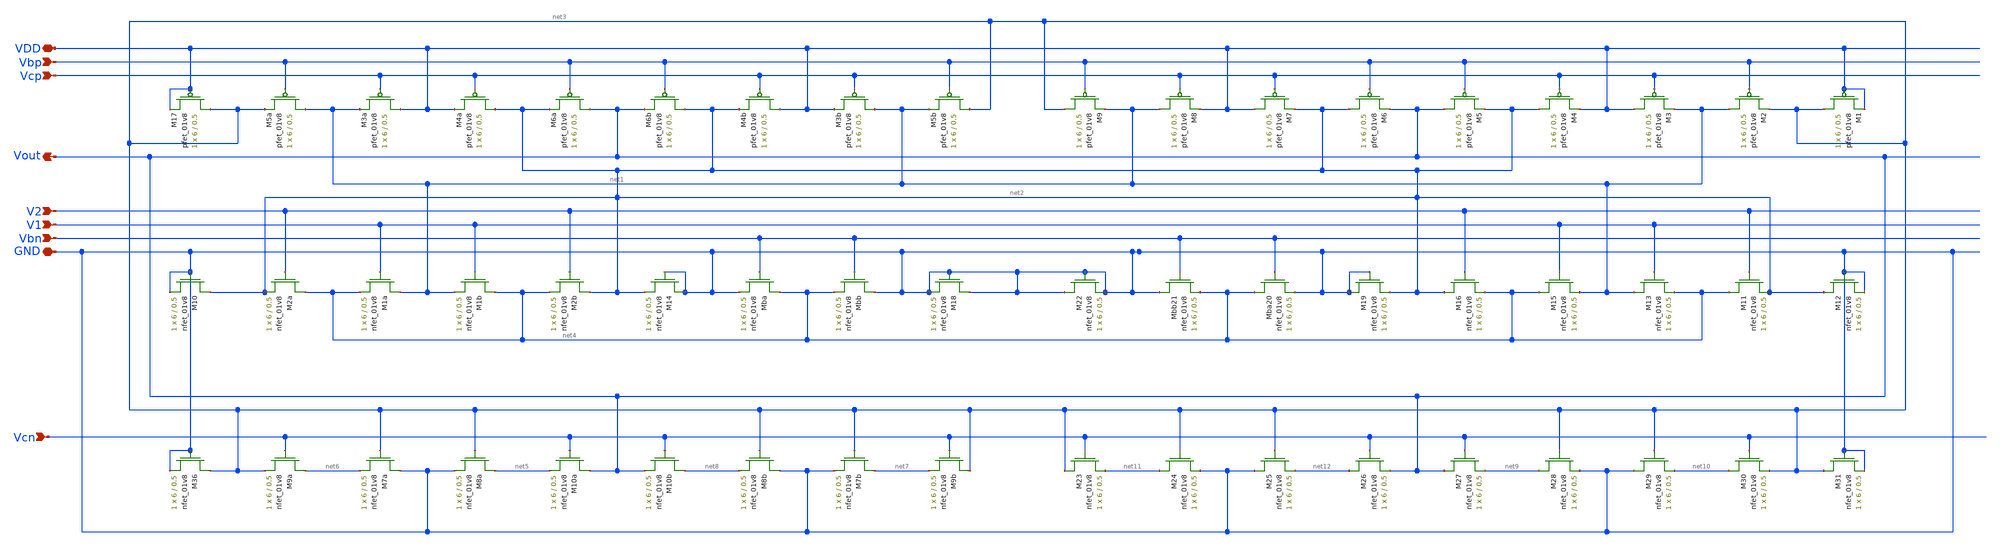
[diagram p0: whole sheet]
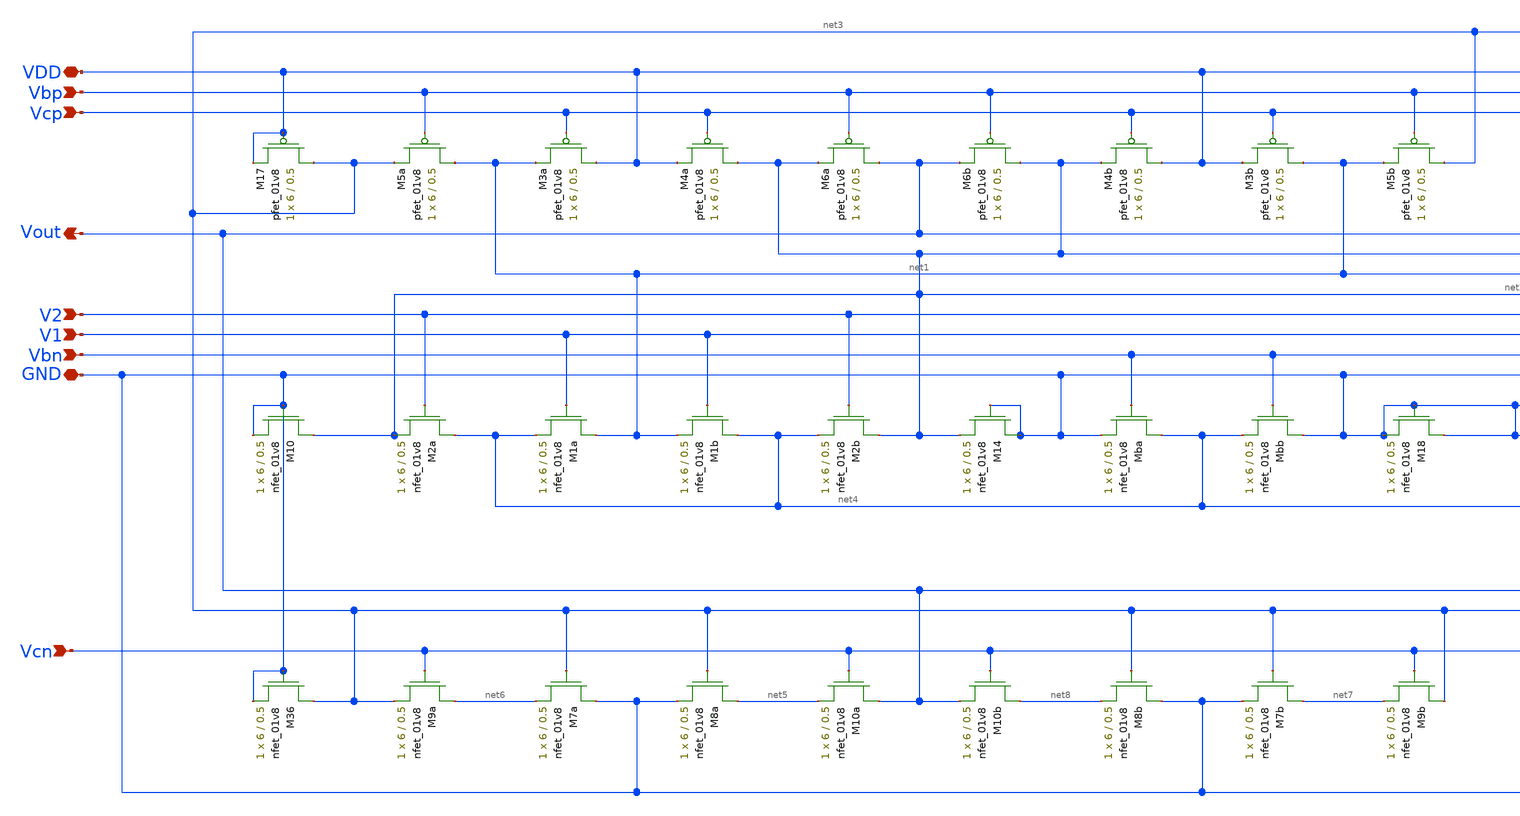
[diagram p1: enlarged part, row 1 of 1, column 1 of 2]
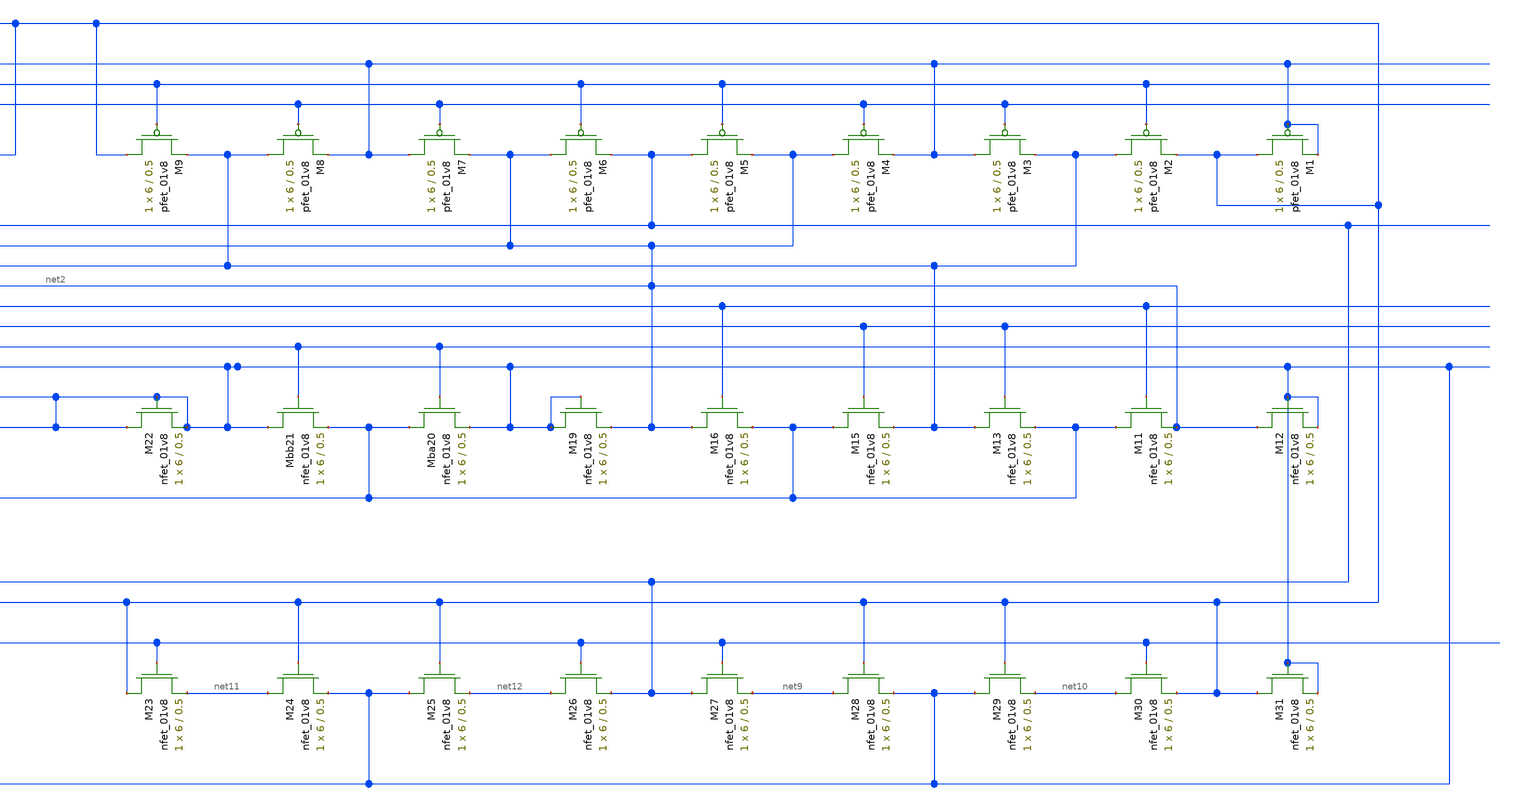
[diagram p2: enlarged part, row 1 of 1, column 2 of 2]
** sch_path: Miniproject3/layout&schematics/LDS_simple.sch
**.subckt LDS_simple Vbp Vout V2 Vbn VDD GND Vcn Vcp V1
*.ipin Vbp
*.opin Vout
*.ipin V2
*.ipin Vbn
*.iopin VDD
*.iopin GND
*.ipin Vcn
*.ipin Vcp
*.ipin V1
XM17 net3 VDD VDD VDD sky130_fd_pr__pfet_01v8 L=0.5 W=6 nf=1 ad='int((nf+1)/2) * W/nf * 0.29' as='int((nf+2)/2) * W/nf * 0.29'
+ pd='2*int((nf+1)/2) * (W/nf + 0.29)' ps='2*int((nf+2)/2) * (W/nf + 0.29)' nrd='0.29 / W' nrs='0.29 / W'
+ sa=0 sb=0 sd=0 mult=1 m=1
XM5a net1 Vbp net3 VDD sky130_fd_pr__pfet_01v8 L=0.5 W=6 nf=1 ad='int((nf+1)/2) * W/nf * 0.29' as='int((nf+2)/2) * W/nf * 0.29'
+ pd='2*int((nf+1)/2) * (W/nf + 0.29)' ps='2*int((nf+2)/2) * (W/nf + 0.29)' nrd='0.29 / W' nrs='0.29 / W'
+ sa=0 sb=0 sd=0 mult=1 m=1
XM3a VDD Vcp net1 VDD sky130_fd_pr__pfet_01v8 L=0.5 W=6 nf=1 ad='int((nf+1)/2) * W/nf * 0.29' as='int((nf+2)/2) * W/nf * 0.29'
+ pd='2*int((nf+1)/2) * (W/nf + 0.29)' ps='2*int((nf+2)/2) * (W/nf + 0.29)' nrd='0.29 / W' nrs='0.29 / W'
+ sa=0 sb=0 sd=0 mult=1 m=1
XM4a net2 Vcp VDD VDD sky130_fd_pr__pfet_01v8 L=0.5 W=6 nf=1 ad='int((nf+1)/2) * W/nf * 0.29' as='int((nf+2)/2) * W/nf * 0.29'
+ pd='2*int((nf+1)/2) * (W/nf + 0.29)' ps='2*int((nf+2)/2) * (W/nf + 0.29)' nrd='0.29 / W' nrs='0.29 / W'
+ sa=0 sb=0 sd=0 mult=1 m=1
XM6a Vout Vbp net2 VDD sky130_fd_pr__pfet_01v8 L=0.5 W=6 nf=1 ad='int((nf+1)/2) * W/nf * 0.29' as='int((nf+2)/2) * W/nf * 0.29'
+ pd='2*int((nf+1)/2) * (W/nf + 0.29)' ps='2*int((nf+2)/2) * (W/nf + 0.29)' nrd='0.29 / W' nrs='0.29 / W'
+ sa=0 sb=0 sd=0 mult=1 m=1
XM6b net2 Vbp Vout VDD sky130_fd_pr__pfet_01v8 L=0.5 W=6 nf=1 ad='int((nf+1)/2) * W/nf * 0.29' as='int((nf+2)/2) * W/nf * 0.29'
+ pd='2*int((nf+1)/2) * (W/nf + 0.29)' ps='2*int((nf+2)/2) * (W/nf + 0.29)' nrd='0.29 / W' nrs='0.29 / W'
+ sa=0 sb=0 sd=0 mult=1 m=1
XM4b VDD Vcp net2 VDD sky130_fd_pr__pfet_01v8 L=0.5 W=6 nf=1 ad='int((nf+1)/2) * W/nf * 0.29' as='int((nf+2)/2) * W/nf * 0.29'
+ pd='2*int((nf+1)/2) * (W/nf + 0.29)' ps='2*int((nf+2)/2) * (W/nf + 0.29)' nrd='0.29 / W' nrs='0.29 / W'
+ sa=0 sb=0 sd=0 mult=1 m=1
XM3b net1 Vcp VDD VDD sky130_fd_pr__pfet_01v8 L=0.5 W=6 nf=1 ad='int((nf+1)/2) * W/nf * 0.29' as='int((nf+2)/2) * W/nf * 0.29'
+ pd='2*int((nf+1)/2) * (W/nf + 0.29)' ps='2*int((nf+2)/2) * (W/nf + 0.29)' nrd='0.29 / W' nrs='0.29 / W'
+ sa=0 sb=0 sd=0 mult=1 m=1
XM5b net3 Vbp net1 VDD sky130_fd_pr__pfet_01v8 L=0.5 W=6 nf=1 ad='int((nf+1)/2) * W/nf * 0.29' as='int((nf+2)/2) * W/nf * 0.29'
+ pd='2*int((nf+1)/2) * (W/nf + 0.29)' ps='2*int((nf+2)/2) * (W/nf + 0.29)' nrd='0.29 / W' nrs='0.29 / W'
+ sa=0 sb=0 sd=0 mult=1 m=1
XM2a net4 V2 net2 GND sky130_fd_pr__nfet_01v8 L=0.5 W=6 nf=1 ad='int((nf+1)/2) * W/nf * 0.29' as='int((nf+2)/2) * W/nf * 0.29'
+ pd='2*int((nf+1)/2) * (W/nf + 0.29)' ps='2*int((nf+2)/2) * (W/nf + 0.29)' nrd='0.29 / W' nrs='0.29 / W'
+ sa=0 sb=0 sd=0 mult=1 m=1
XM10 net2 GND GND GND sky130_fd_pr__nfet_01v8 L=0.5 W=6 nf=1 ad='int((nf+1)/2) * W/nf * 0.29' as='int((nf+2)/2) * W/nf * 0.29'
+ pd='2*int((nf+1)/2) * (W/nf + 0.29)' ps='2*int((nf+2)/2) * (W/nf + 0.29)' nrd='0.29 / W' nrs='0.29 / W'
+ sa=0 sb=0 sd=0 mult=1 m=1
XM1a net1 V1 net4 GND sky130_fd_pr__nfet_01v8 L=0.5 W=6 nf=1 ad='int((nf+1)/2) * W/nf * 0.29' as='int((nf+2)/2) * W/nf * 0.29'
+ pd='2*int((nf+1)/2) * (W/nf + 0.29)' ps='2*int((nf+2)/2) * (W/nf + 0.29)' nrd='0.29 / W' nrs='0.29 / W'
+ sa=0 sb=0 sd=0 mult=1 m=1
XM1b net4 V1 net1 GND sky130_fd_pr__nfet_01v8 L=0.5 W=6 nf=1 ad='int((nf+1)/2) * W/nf * 0.29' as='int((nf+2)/2) * W/nf * 0.29'
+ pd='2*int((nf+1)/2) * (W/nf + 0.29)' ps='2*int((nf+2)/2) * (W/nf + 0.29)' nrd='0.29 / W' nrs='0.29 / W'
+ sa=0 sb=0 sd=0 mult=1 m=1
XM2b net2 V2 net4 GND sky130_fd_pr__nfet_01v8 L=0.5 W=6 nf=1 ad='int((nf+1)/2) * W/nf * 0.29' as='int((nf+2)/2) * W/nf * 0.29'
+ pd='2*int((nf+1)/2) * (W/nf + 0.29)' ps='2*int((nf+2)/2) * (W/nf + 0.29)' nrd='0.29 / W' nrs='0.29 / W'
+ sa=0 sb=0 sd=0 mult=1 m=1
XM14 GND GND net2 GND sky130_fd_pr__nfet_01v8 L=0.5 W=6 nf=1 ad='int((nf+1)/2) * W/nf * 0.29' as='int((nf+2)/2) * W/nf * 0.29'
+ pd='2*int((nf+1)/2) * (W/nf + 0.29)' ps='2*int((nf+2)/2) * (W/nf + 0.29)' nrd='0.29 / W' nrs='0.29 / W'
+ sa=0 sb=0 sd=0 mult=1 m=1
XMba net4 Vbn GND GND sky130_fd_pr__nfet_01v8 L=0.5 W=6 nf=1 ad='int((nf+1)/2) * W/nf * 0.29' as='int((nf+2)/2) * W/nf * 0.29'
+ pd='2*int((nf+1)/2) * (W/nf + 0.29)' ps='2*int((nf+2)/2) * (W/nf + 0.29)' nrd='0.29 / W' nrs='0.29 / W'
+ sa=0 sb=0 sd=0 mult=1 m=1
XMbb GND Vbn net4 GND sky130_fd_pr__nfet_01v8 L=0.5 W=6 nf=1 ad='int((nf+1)/2) * W/nf * 0.29' as='int((nf+2)/2) * W/nf * 0.29'
+ pd='2*int((nf+1)/2) * (W/nf + 0.29)' ps='2*int((nf+2)/2) * (W/nf + 0.29)' nrd='0.29 / W' nrs='0.29 / W'
+ sa=0 sb=0 sd=0 mult=1 m=1
XM18 GND GND GND GND sky130_fd_pr__nfet_01v8 L=0.5 W=6 nf=1 ad='int((nf+1)/2) * W/nf * 0.29' as='int((nf+2)/2) * W/nf * 0.29'
+ pd='2*int((nf+1)/2) * (W/nf + 0.29)' ps='2*int((nf+2)/2) * (W/nf + 0.29)' nrd='0.29 / W' nrs='0.29 / W'
+ sa=0 sb=0 sd=0 mult=1 m=1
XM9b net3 Vcn net7 GND sky130_fd_pr__nfet_01v8 L=0.5 W=6 nf=1 ad='int((nf+1)/2) * W/nf * 0.29' as='int((nf+2)/2) * W/nf * 0.29'
+ pd='2*int((nf+1)/2) * (W/nf + 0.29)' ps='2*int((nf+2)/2) * (W/nf + 0.29)' nrd='0.29 / W' nrs='0.29 / W'
+ sa=0 sb=0 sd=0 mult=1 m=1
XM7b net7 net3 GND GND sky130_fd_pr__nfet_01v8 L=0.5 W=6 nf=1 ad='int((nf+1)/2) * W/nf * 0.29' as='int((nf+2)/2) * W/nf * 0.29'
+ pd='2*int((nf+1)/2) * (W/nf + 0.29)' ps='2*int((nf+2)/2) * (W/nf + 0.29)' nrd='0.29 / W' nrs='0.29 / W'
+ sa=0 sb=0 sd=0 mult=1 m=1
XM8b GND net3 net8 GND sky130_fd_pr__nfet_01v8 L=0.5 W=6 nf=1 ad='int((nf+1)/2) * W/nf * 0.29' as='int((nf+2)/2) * W/nf * 0.29'
+ pd='2*int((nf+1)/2) * (W/nf + 0.29)' ps='2*int((nf+2)/2) * (W/nf + 0.29)' nrd='0.29 / W' nrs='0.29 / W'
+ sa=0 sb=0 sd=0 mult=1 m=1
XM10b net8 Vcn Vout GND sky130_fd_pr__nfet_01v8 L=0.5 W=6 nf=1 ad='int((nf+1)/2) * W/nf * 0.29' as='int((nf+2)/2) * W/nf * 0.29'
+ pd='2*int((nf+1)/2) * (W/nf + 0.29)' ps='2*int((nf+2)/2) * (W/nf + 0.29)' nrd='0.29 / W' nrs='0.29 / W'
+ sa=0 sb=0 sd=0 mult=1 m=1
XM10a Vout Vcn net5 GND sky130_fd_pr__nfet_01v8 L=0.5 W=6 nf=1 ad='int((nf+1)/2) * W/nf * 0.29' as='int((nf+2)/2) * W/nf * 0.29'
+ pd='2*int((nf+1)/2) * (W/nf + 0.29)' ps='2*int((nf+2)/2) * (W/nf + 0.29)' nrd='0.29 / W' nrs='0.29 / W'
+ sa=0 sb=0 sd=0 mult=1 m=1
XM8a net5 net3 GND GND sky130_fd_pr__nfet_01v8 L=0.5 W=6 nf=1 ad='int((nf+1)/2) * W/nf * 0.29' as='int((nf+2)/2) * W/nf * 0.29'
+ pd='2*int((nf+1)/2) * (W/nf + 0.29)' ps='2*int((nf+2)/2) * (W/nf + 0.29)' nrd='0.29 / W' nrs='0.29 / W'
+ sa=0 sb=0 sd=0 mult=1 m=1
XM7a GND net3 net6 GND sky130_fd_pr__nfet_01v8 L=0.5 W=6 nf=1 ad='int((nf+1)/2) * W/nf * 0.29' as='int((nf+2)/2) * W/nf * 0.29'
+ pd='2*int((nf+1)/2) * (W/nf + 0.29)' ps='2*int((nf+2)/2) * (W/nf + 0.29)' nrd='0.29 / W' nrs='0.29 / W'
+ sa=0 sb=0 sd=0 mult=1 m=1
XM9a net6 Vcn net3 GND sky130_fd_pr__nfet_01v8 L=0.5 W=6 nf=1 ad='int((nf+1)/2) * W/nf * 0.29' as='int((nf+2)/2) * W/nf * 0.29'
+ pd='2*int((nf+1)/2) * (W/nf + 0.29)' ps='2*int((nf+2)/2) * (W/nf + 0.29)' nrd='0.29 / W' nrs='0.29 / W'
+ sa=0 sb=0 sd=0 mult=1 m=1
XM36 net3 GND GND GND sky130_fd_pr__nfet_01v8 L=0.5 W=6 nf=1 ad='int((nf+1)/2) * W/nf * 0.29' as='int((nf+2)/2) * W/nf * 0.29'
+ pd='2*int((nf+1)/2) * (W/nf + 0.29)' ps='2*int((nf+2)/2) * (W/nf + 0.29)' nrd='0.29 / W' nrs='0.29 / W'
+ sa=0 sb=0 sd=0 mult=1 m=1
XM1 net3 VDD VDD VDD sky130_fd_pr__pfet_01v8 L=0.5 W=6 nf=1 ad='int((nf+1)/2) * W/nf * 0.29' as='int((nf+2)/2) * W/nf * 0.29'
+ pd='2*int((nf+1)/2) * (W/nf + 0.29)' ps='2*int((nf+2)/2) * (W/nf + 0.29)' nrd='0.29 / W' nrs='0.29 / W'
+ sa=0 sb=0 sd=0 mult=1 m=1
XM2 net1 Vbp net3 VDD sky130_fd_pr__pfet_01v8 L=0.5 W=6 nf=1 ad='int((nf+1)/2) * W/nf * 0.29' as='int((nf+2)/2) * W/nf * 0.29'
+ pd='2*int((nf+1)/2) * (W/nf + 0.29)' ps='2*int((nf+2)/2) * (W/nf + 0.29)' nrd='0.29 / W' nrs='0.29 / W'
+ sa=0 sb=0 sd=0 mult=1 m=1
XM3 VDD Vcp net1 VDD sky130_fd_pr__pfet_01v8 L=0.5 W=6 nf=1 ad='int((nf+1)/2) * W/nf * 0.29' as='int((nf+2)/2) * W/nf * 0.29'
+ pd='2*int((nf+1)/2) * (W/nf + 0.29)' ps='2*int((nf+2)/2) * (W/nf + 0.29)' nrd='0.29 / W' nrs='0.29 / W'
+ sa=0 sb=0 sd=0 mult=1 m=1
XM4 net2 Vcp VDD VDD sky130_fd_pr__pfet_01v8 L=0.5 W=6 nf=1 ad='int((nf+1)/2) * W/nf * 0.29' as='int((nf+2)/2) * W/nf * 0.29'
+ pd='2*int((nf+1)/2) * (W/nf + 0.29)' ps='2*int((nf+2)/2) * (W/nf + 0.29)' nrd='0.29 / W' nrs='0.29 / W'
+ sa=0 sb=0 sd=0 mult=1 m=1
XM5 Vout Vbp net2 VDD sky130_fd_pr__pfet_01v8 L=0.5 W=6 nf=1 ad='int((nf+1)/2) * W/nf * 0.29' as='int((nf+2)/2) * W/nf * 0.29'
+ pd='2*int((nf+1)/2) * (W/nf + 0.29)' ps='2*int((nf+2)/2) * (W/nf + 0.29)' nrd='0.29 / W' nrs='0.29 / W'
+ sa=0 sb=0 sd=0 mult=1 m=1
XM6 net2 Vbp Vout VDD sky130_fd_pr__pfet_01v8 L=0.5 W=6 nf=1 ad='int((nf+1)/2) * W/nf * 0.29' as='int((nf+2)/2) * W/nf * 0.29'
+ pd='2*int((nf+1)/2) * (W/nf + 0.29)' ps='2*int((nf+2)/2) * (W/nf + 0.29)' nrd='0.29 / W' nrs='0.29 / W'
+ sa=0 sb=0 sd=0 mult=1 m=1
XM7 VDD Vcp net2 VDD sky130_fd_pr__pfet_01v8 L=0.5 W=6 nf=1 ad='int((nf+1)/2) * W/nf * 0.29' as='int((nf+2)/2) * W/nf * 0.29'
+ pd='2*int((nf+1)/2) * (W/nf + 0.29)' ps='2*int((nf+2)/2) * (W/nf + 0.29)' nrd='0.29 / W' nrs='0.29 / W'
+ sa=0 sb=0 sd=0 mult=1 m=1
XM8 net1 Vcp VDD VDD sky130_fd_pr__pfet_01v8 L=0.5 W=6 nf=1 ad='int((nf+1)/2) * W/nf * 0.29' as='int((nf+2)/2) * W/nf * 0.29'
+ pd='2*int((nf+1)/2) * (W/nf + 0.29)' ps='2*int((nf+2)/2) * (W/nf + 0.29)' nrd='0.29 / W' nrs='0.29 / W'
+ sa=0 sb=0 sd=0 mult=1 m=1
XM9 net3 Vbp net1 VDD sky130_fd_pr__pfet_01v8 L=0.5 W=6 nf=1 ad='int((nf+1)/2) * W/nf * 0.29' as='int((nf+2)/2) * W/nf * 0.29'
+ pd='2*int((nf+1)/2) * (W/nf + 0.29)' ps='2*int((nf+2)/2) * (W/nf + 0.29)' nrd='0.29 / W' nrs='0.29 / W'
+ sa=0 sb=0 sd=0 mult=1 m=1
XM11 net4 V2 net2 GND sky130_fd_pr__nfet_01v8 L=0.5 W=6 nf=1 ad='int((nf+1)/2) * W/nf * 0.29' as='int((nf+2)/2) * W/nf * 0.29'
+ pd='2*int((nf+1)/2) * (W/nf + 0.29)' ps='2*int((nf+2)/2) * (W/nf + 0.29)' nrd='0.29 / W' nrs='0.29 / W'
+ sa=0 sb=0 sd=0 mult=1 m=1
XM12 net2 GND GND GND sky130_fd_pr__nfet_01v8 L=0.5 W=6 nf=1 ad='int((nf+1)/2) * W/nf * 0.29' as='int((nf+2)/2) * W/nf * 0.29'
+ pd='2*int((nf+1)/2) * (W/nf + 0.29)' ps='2*int((nf+2)/2) * (W/nf + 0.29)' nrd='0.29 / W' nrs='0.29 / W'
+ sa=0 sb=0 sd=0 mult=1 m=1
XM13 net1 V1 net4 GND sky130_fd_pr__nfet_01v8 L=0.5 W=6 nf=1 ad='int((nf+1)/2) * W/nf * 0.29' as='int((nf+2)/2) * W/nf * 0.29'
+ pd='2*int((nf+1)/2) * (W/nf + 0.29)' ps='2*int((nf+2)/2) * (W/nf + 0.29)' nrd='0.29 / W' nrs='0.29 / W'
+ sa=0 sb=0 sd=0 mult=1 m=1
XM15 net4 V1 net1 GND sky130_fd_pr__nfet_01v8 L=0.5 W=6 nf=1 ad='int((nf+1)/2) * W/nf * 0.29' as='int((nf+2)/2) * W/nf * 0.29'
+ pd='2*int((nf+1)/2) * (W/nf + 0.29)' ps='2*int((nf+2)/2) * (W/nf + 0.29)' nrd='0.29 / W' nrs='0.29 / W'
+ sa=0 sb=0 sd=0 mult=1 m=1
XM16 net2 V2 net4 GND sky130_fd_pr__nfet_01v8 L=0.5 W=6 nf=1 ad='int((nf+1)/2) * W/nf * 0.29' as='int((nf+2)/2) * W/nf * 0.29'
+ pd='2*int((nf+1)/2) * (W/nf + 0.29)' ps='2*int((nf+2)/2) * (W/nf + 0.29)' nrd='0.29 / W' nrs='0.29 / W'
+ sa=0 sb=0 sd=0 mult=1 m=1
XM19 GND GND net2 GND sky130_fd_pr__nfet_01v8 L=0.5 W=6 nf=1 ad='int((nf+1)/2) * W/nf * 0.29' as='int((nf+2)/2) * W/nf * 0.29'
+ pd='2*int((nf+1)/2) * (W/nf + 0.29)' ps='2*int((nf+2)/2) * (W/nf + 0.29)' nrd='0.29 / W' nrs='0.29 / W'
+ sa=0 sb=0 sd=0 mult=1 m=1
XMba20 net4 Vbn GND GND sky130_fd_pr__nfet_01v8 L=0.5 W=6 nf=1 ad='int((nf+1)/2) * W/nf * 0.29' as='int((nf+2)/2) * W/nf * 0.29'
+ pd='2*int((nf+1)/2) * (W/nf + 0.29)' ps='2*int((nf+2)/2) * (W/nf + 0.29)' nrd='0.29 / W' nrs='0.29 / W'
+ sa=0 sb=0 sd=0 mult=1 m=1
XMbb21 GND Vbn net4 GND sky130_fd_pr__nfet_01v8 L=0.5 W=6 nf=1 ad='int((nf+1)/2) * W/nf * 0.29' as='int((nf+2)/2) * W/nf * 0.29'
+ pd='2*int((nf+1)/2) * (W/nf + 0.29)' ps='2*int((nf+2)/2) * (W/nf + 0.29)' nrd='0.29 / W' nrs='0.29 / W'
+ sa=0 sb=0 sd=0 mult=1 m=1
XM22 GND GND GND GND sky130_fd_pr__nfet_01v8 L=0.5 W=6 nf=1 ad='int((nf+1)/2) * W/nf * 0.29' as='int((nf+2)/2) * W/nf * 0.29'
+ pd='2*int((nf+1)/2) * (W/nf + 0.29)' ps='2*int((nf+2)/2) * (W/nf + 0.29)' nrd='0.29 / W' nrs='0.29 / W'
+ sa=0 sb=0 sd=0 mult=1 m=1
XM23 net3 Vcn net11 GND sky130_fd_pr__nfet_01v8 L=0.5 W=6 nf=1 ad='int((nf+1)/2) * W/nf * 0.29' as='int((nf+2)/2) * W/nf * 0.29'
+ pd='2*int((nf+1)/2) * (W/nf + 0.29)' ps='2*int((nf+2)/2) * (W/nf + 0.29)' nrd='0.29 / W' nrs='0.29 / W'
+ sa=0 sb=0 sd=0 mult=1 m=1
XM24 net11 net3 GND GND sky130_fd_pr__nfet_01v8 L=0.5 W=6 nf=1 ad='int((nf+1)/2) * W/nf * 0.29' as='int((nf+2)/2) * W/nf * 0.29'
+ pd='2*int((nf+1)/2) * (W/nf + 0.29)' ps='2*int((nf+2)/2) * (W/nf + 0.29)' nrd='0.29 / W' nrs='0.29 / W'
+ sa=0 sb=0 sd=0 mult=1 m=1
XM25 GND net3 net12 GND sky130_fd_pr__nfet_01v8 L=0.5 W=6 nf=1 ad='int((nf+1)/2) * W/nf * 0.29' as='int((nf+2)/2) * W/nf * 0.29'
+ pd='2*int((nf+1)/2) * (W/nf + 0.29)' ps='2*int((nf+2)/2) * (W/nf + 0.29)' nrd='0.29 / W' nrs='0.29 / W'
+ sa=0 sb=0 sd=0 mult=1 m=1
XM26 net12 Vcn Vout GND sky130_fd_pr__nfet_01v8 L=0.5 W=6 nf=1 ad='int((nf+1)/2) * W/nf * 0.29' as='int((nf+2)/2) * W/nf * 0.29'
+ pd='2*int((nf+1)/2) * (W/nf + 0.29)' ps='2*int((nf+2)/2) * (W/nf + 0.29)' nrd='0.29 / W' nrs='0.29 / W'
+ sa=0 sb=0 sd=0 mult=1 m=1
XM27 Vout Vcn net9 GND sky130_fd_pr__nfet_01v8 L=0.5 W=6 nf=1 ad='int((nf+1)/2) * W/nf * 0.29' as='int((nf+2)/2) * W/nf * 0.29'
+ pd='2*int((nf+1)/2) * (W/nf + 0.29)' ps='2*int((nf+2)/2) * (W/nf + 0.29)' nrd='0.29 / W' nrs='0.29 / W'
+ sa=0 sb=0 sd=0 mult=1 m=1
XM28 net9 net3 GND GND sky130_fd_pr__nfet_01v8 L=0.5 W=6 nf=1 ad='int((nf+1)/2) * W/nf * 0.29' as='int((nf+2)/2) * W/nf * 0.29'
+ pd='2*int((nf+1)/2) * (W/nf + 0.29)' ps='2*int((nf+2)/2) * (W/nf + 0.29)' nrd='0.29 / W' nrs='0.29 / W'
+ sa=0 sb=0 sd=0 mult=1 m=1
XM29 GND net3 net10 GND sky130_fd_pr__nfet_01v8 L=0.5 W=6 nf=1 ad='int((nf+1)/2) * W/nf * 0.29' as='int((nf+2)/2) * W/nf * 0.29'
+ pd='2*int((nf+1)/2) * (W/nf + 0.29)' ps='2*int((nf+2)/2) * (W/nf + 0.29)' nrd='0.29 / W' nrs='0.29 / W'
+ sa=0 sb=0 sd=0 mult=1 m=1
XM30 net10 Vcn net3 GND sky130_fd_pr__nfet_01v8 L=0.5 W=6 nf=1 ad='int((nf+1)/2) * W/nf * 0.29' as='int((nf+2)/2) * W/nf * 0.29'
+ pd='2*int((nf+1)/2) * (W/nf + 0.29)' ps='2*int((nf+2)/2) * (W/nf + 0.29)' nrd='0.29 / W' nrs='0.29 / W'
+ sa=0 sb=0 sd=0 mult=1 m=1
XM31 net3 GND GND GND sky130_fd_pr__nfet_01v8 L=0.5 W=6 nf=1 ad='int((nf+1)/2) * W/nf * 0.29' as='int((nf+2)/2) * W/nf * 0.29'
+ pd='2*int((nf+1)/2) * (W/nf + 0.29)' ps='2*int((nf+2)/2) * (W/nf + 0.29)' nrd='0.29 / W' nrs='0.29 / W'
+ sa=0 sb=0 sd=0 mult=1 m=1
**.ends
.end
